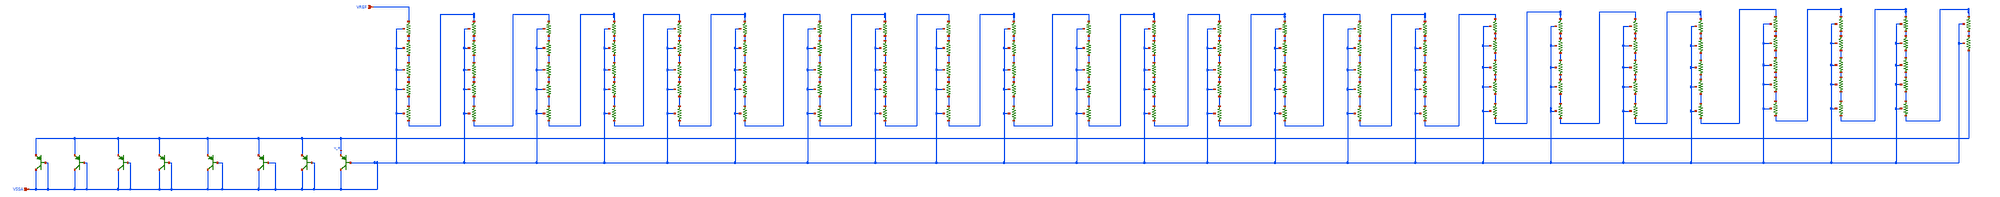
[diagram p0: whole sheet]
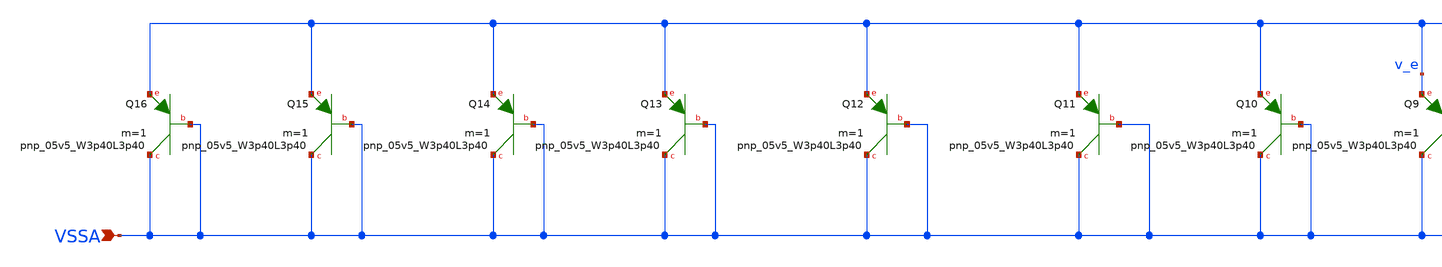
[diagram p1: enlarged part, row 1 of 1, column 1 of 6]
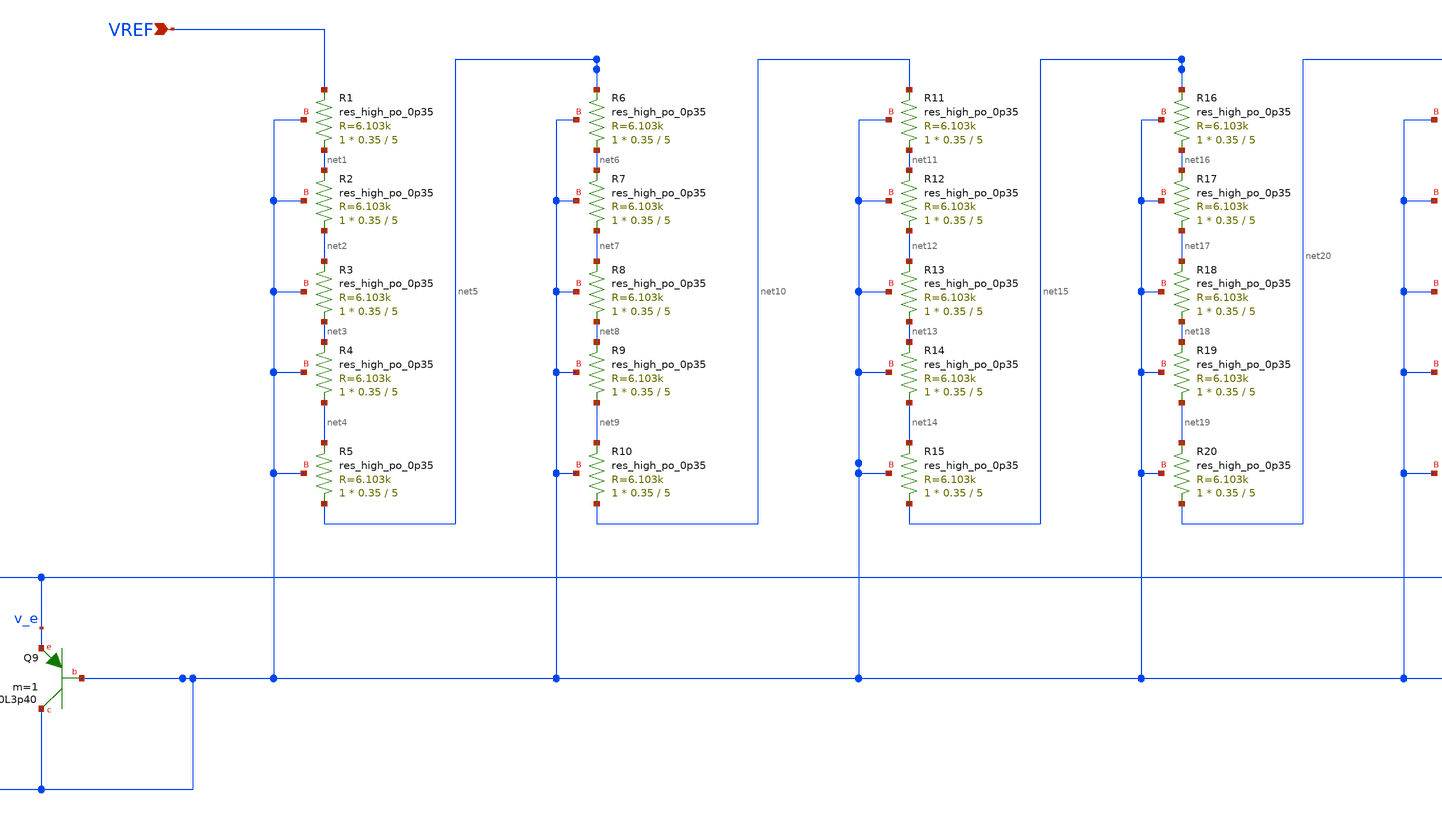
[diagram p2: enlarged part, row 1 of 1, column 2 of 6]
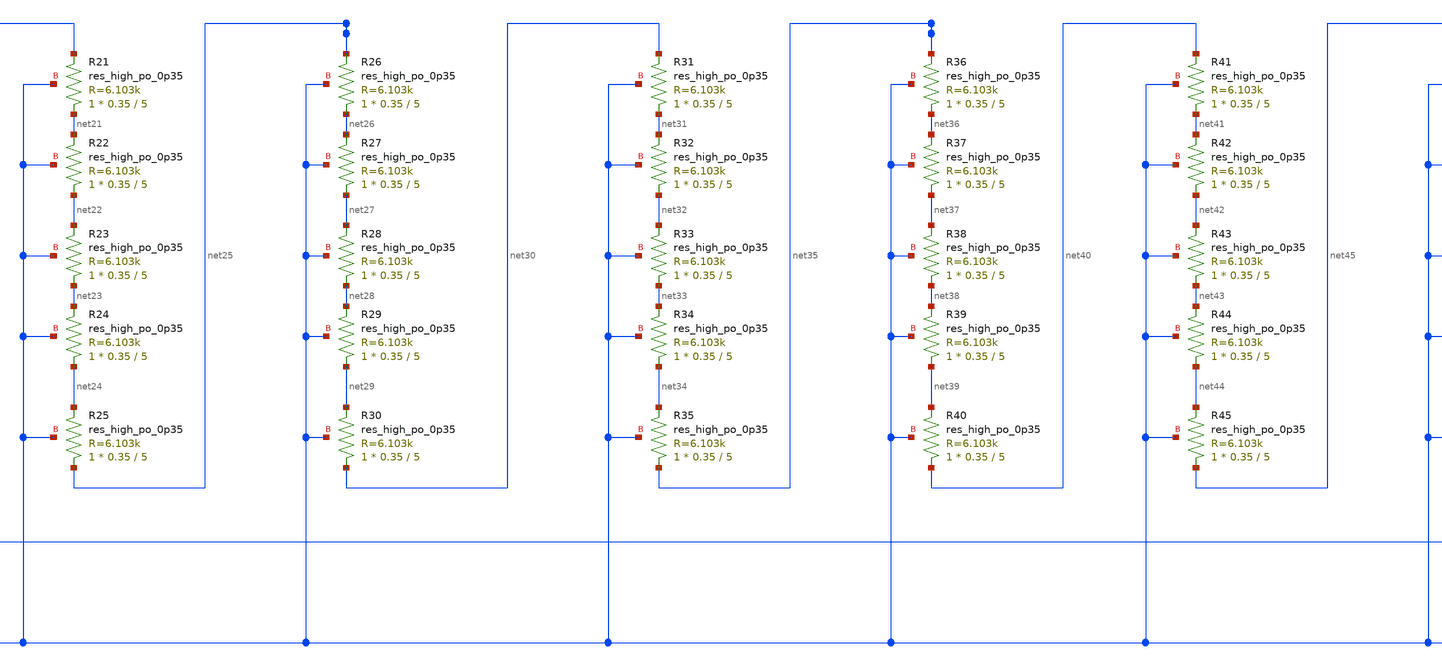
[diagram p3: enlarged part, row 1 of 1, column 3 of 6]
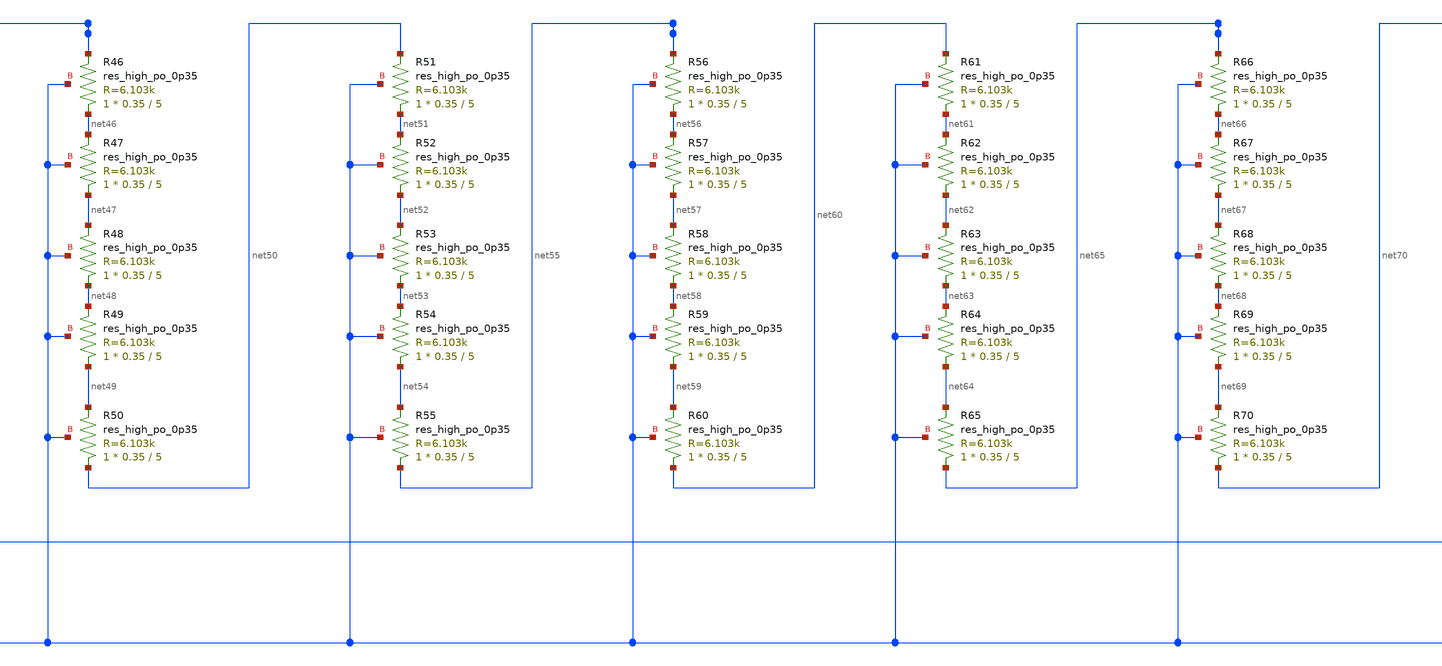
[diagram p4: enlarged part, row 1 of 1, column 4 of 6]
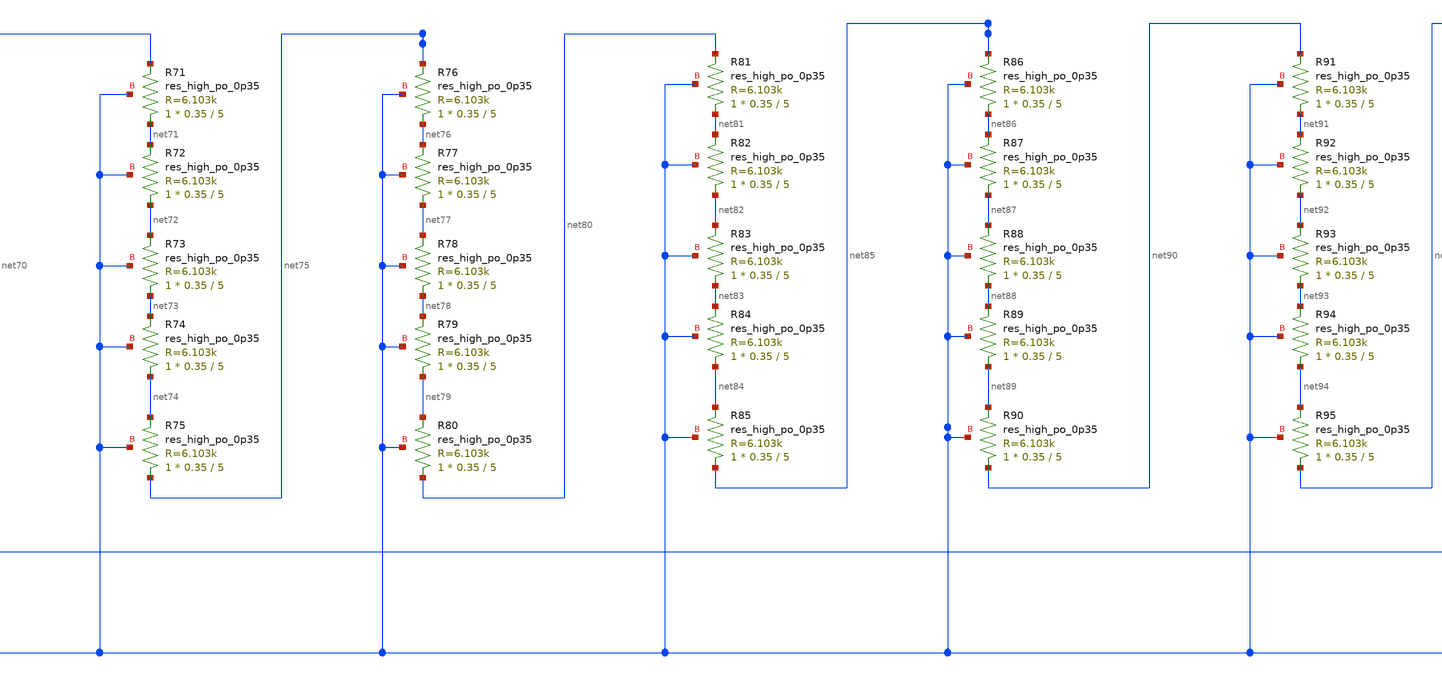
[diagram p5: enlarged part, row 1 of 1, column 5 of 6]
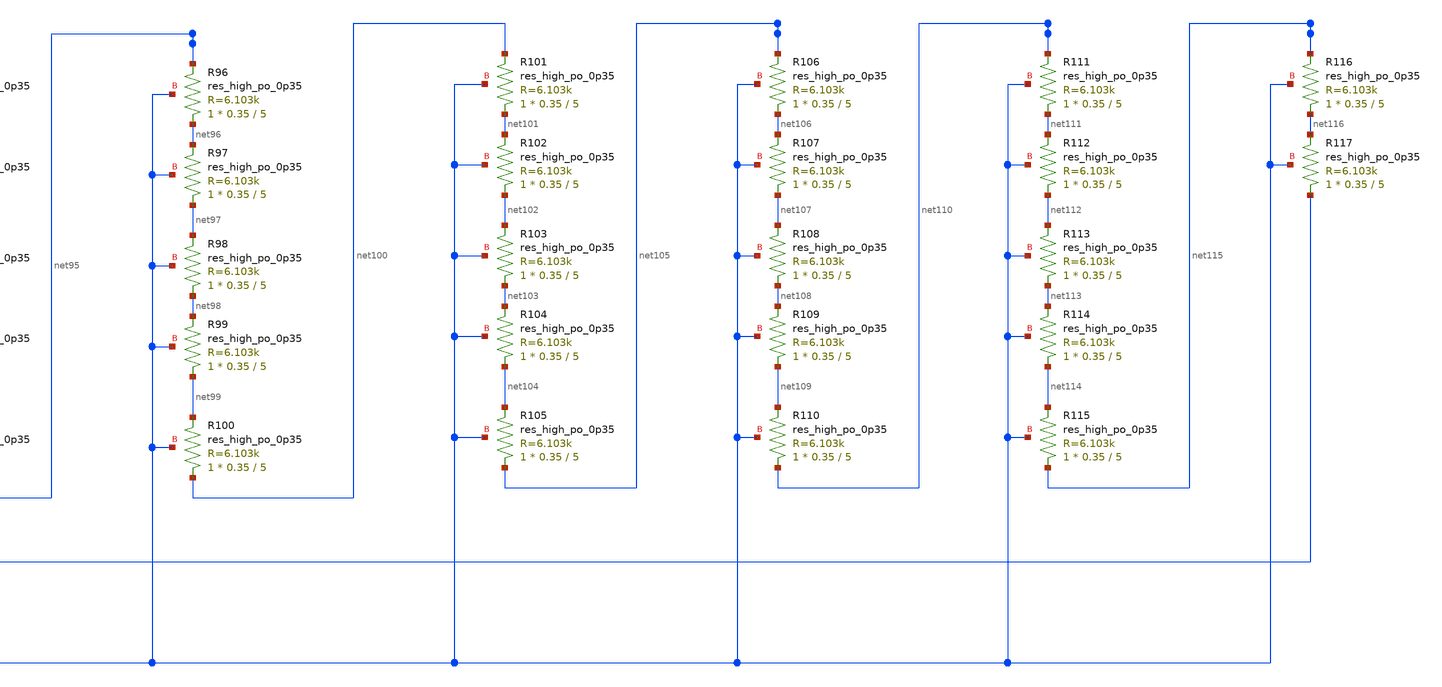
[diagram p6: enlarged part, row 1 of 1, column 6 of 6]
** sch_path: gds/bg2_right_branch_lvs.sch
**.subckt bg2_right_branch_lvs VSSA VREF
*.ipin VSSA
*.ipin VREF
XQ9 VSSA VSSA v_e sky130_fd_pr__pnp_05v5_W3p40L3p40 m=1
XQ10 VSSA VSSA v_e sky130_fd_pr__pnp_05v5_W3p40L3p40 m=1
XQ11 VSSA VSSA v_e sky130_fd_pr__pnp_05v5_W3p40L3p40 m=1
XQ12 VSSA VSSA v_e sky130_fd_pr__pnp_05v5_W3p40L3p40 m=1
XQ13 VSSA VSSA v_e sky130_fd_pr__pnp_05v5_W3p40L3p40 m=1
XQ14 VSSA VSSA v_e sky130_fd_pr__pnp_05v5_W3p40L3p40 m=1
XQ15 VSSA VSSA v_e sky130_fd_pr__pnp_05v5_W3p40L3p40 m=1
XQ16 VSSA VSSA v_e sky130_fd_pr__pnp_05v5_W3p40L3p40 m=1
XR1 net1 VREF VSSA sky130_fd_pr__res_high_po_0p35 L=5 mult=1 m=1
XR2 net2 net1 VSSA sky130_fd_pr__res_high_po_0p35 L=5 mult=1 m=1
XR3 net3 net2 VSSA sky130_fd_pr__res_high_po_0p35 L=5 mult=1 m=1
XR4 net4 net3 VSSA sky130_fd_pr__res_high_po_0p35 L=5 mult=1 m=1
XR5 net5 net4 VSSA sky130_fd_pr__res_high_po_0p35 L=5 mult=1 m=1
XR6 net6 net5 VSSA sky130_fd_pr__res_high_po_0p35 L=5 mult=1 m=1
XR7 net7 net6 VSSA sky130_fd_pr__res_high_po_0p35 L=5 mult=1 m=1
XR8 net8 net7 VSSA sky130_fd_pr__res_high_po_0p35 L=5 mult=1 m=1
XR9 net9 net8 VSSA sky130_fd_pr__res_high_po_0p35 L=5 mult=1 m=1
XR10 net10 net9 VSSA sky130_fd_pr__res_high_po_0p35 L=5 mult=1 m=1
XR11 net11 net10 VSSA sky130_fd_pr__res_high_po_0p35 L=5 mult=1 m=1
XR12 net12 net11 VSSA sky130_fd_pr__res_high_po_0p35 L=5 mult=1 m=1
XR13 net13 net12 VSSA sky130_fd_pr__res_high_po_0p35 L=5 mult=1 m=1
XR14 net14 net13 VSSA sky130_fd_pr__res_high_po_0p35 L=5 mult=1 m=1
XR15 net15 net14 VSSA sky130_fd_pr__res_high_po_0p35 L=5 mult=1 m=1
XR16 net16 net15 VSSA sky130_fd_pr__res_high_po_0p35 L=5 mult=1 m=1
XR17 net17 net16 VSSA sky130_fd_pr__res_high_po_0p35 L=5 mult=1 m=1
XR18 net18 net17 VSSA sky130_fd_pr__res_high_po_0p35 L=5 mult=1 m=1
XR19 net19 net18 VSSA sky130_fd_pr__res_high_po_0p35 L=5 mult=1 m=1
XR20 net20 net19 VSSA sky130_fd_pr__res_high_po_0p35 L=5 mult=1 m=1
XR21 net21 net20 VSSA sky130_fd_pr__res_high_po_0p35 L=5 mult=1 m=1
XR22 net22 net21 VSSA sky130_fd_pr__res_high_po_0p35 L=5 mult=1 m=1
XR23 net23 net22 VSSA sky130_fd_pr__res_high_po_0p35 L=5 mult=1 m=1
XR24 net24 net23 VSSA sky130_fd_pr__res_high_po_0p35 L=5 mult=1 m=1
XR25 net25 net24 VSSA sky130_fd_pr__res_high_po_0p35 L=5 mult=1 m=1
XR26 net26 net25 VSSA sky130_fd_pr__res_high_po_0p35 L=5 mult=1 m=1
XR27 net27 net26 VSSA sky130_fd_pr__res_high_po_0p35 L=5 mult=1 m=1
XR28 net28 net27 VSSA sky130_fd_pr__res_high_po_0p35 L=5 mult=1 m=1
XR29 net29 net28 VSSA sky130_fd_pr__res_high_po_0p35 L=5 mult=1 m=1
XR30 net30 net29 VSSA sky130_fd_pr__res_high_po_0p35 L=5 mult=1 m=1
XR31 net31 net30 VSSA sky130_fd_pr__res_high_po_0p35 L=5 mult=1 m=1
XR32 net32 net31 VSSA sky130_fd_pr__res_high_po_0p35 L=5 mult=1 m=1
XR33 net33 net32 VSSA sky130_fd_pr__res_high_po_0p35 L=5 mult=1 m=1
XR34 net34 net33 VSSA sky130_fd_pr__res_high_po_0p35 L=5 mult=1 m=1
XR35 net35 net34 VSSA sky130_fd_pr__res_high_po_0p35 L=5 mult=1 m=1
XR36 net36 net35 VSSA sky130_fd_pr__res_high_po_0p35 L=5 mult=1 m=1
XR37 net37 net36 VSSA sky130_fd_pr__res_high_po_0p35 L=5 mult=1 m=1
XR38 net38 net37 VSSA sky130_fd_pr__res_high_po_0p35 L=5 mult=1 m=1
XR39 net39 net38 VSSA sky130_fd_pr__res_high_po_0p35 L=5 mult=1 m=1
XR40 net40 net39 VSSA sky130_fd_pr__res_high_po_0p35 L=5 mult=1 m=1
XR41 net41 net40 VSSA sky130_fd_pr__res_high_po_0p35 L=5 mult=1 m=1
XR42 net42 net41 VSSA sky130_fd_pr__res_high_po_0p35 L=5 mult=1 m=1
XR43 net43 net42 VSSA sky130_fd_pr__res_high_po_0p35 L=5 mult=1 m=1
XR44 net44 net43 VSSA sky130_fd_pr__res_high_po_0p35 L=5 mult=1 m=1
XR45 net45 net44 VSSA sky130_fd_pr__res_high_po_0p35 L=5 mult=1 m=1
XR46 net46 net45 VSSA sky130_fd_pr__res_high_po_0p35 L=5 mult=1 m=1
XR47 net47 net46 VSSA sky130_fd_pr__res_high_po_0p35 L=5 mult=1 m=1
XR48 net48 net47 VSSA sky130_fd_pr__res_high_po_0p35 L=5 mult=1 m=1
XR49 net49 net48 VSSA sky130_fd_pr__res_high_po_0p35 L=5 mult=1 m=1
XR50 net50 net49 VSSA sky130_fd_pr__res_high_po_0p35 L=5 mult=1 m=1
XR51 net51 net50 VSSA sky130_fd_pr__res_high_po_0p35 L=5 mult=1 m=1
XR52 net52 net51 VSSA sky130_fd_pr__res_high_po_0p35 L=5 mult=1 m=1
XR53 net53 net52 VSSA sky130_fd_pr__res_high_po_0p35 L=5 mult=1 m=1
XR54 net54 net53 VSSA sky130_fd_pr__res_high_po_0p35 L=5 mult=1 m=1
XR55 net55 net54 VSSA sky130_fd_pr__res_high_po_0p35 L=5 mult=1 m=1
XR56 net56 net55 VSSA sky130_fd_pr__res_high_po_0p35 L=5 mult=1 m=1
XR57 net57 net56 VSSA sky130_fd_pr__res_high_po_0p35 L=5 mult=1 m=1
XR58 net58 net57 VSSA sky130_fd_pr__res_high_po_0p35 L=5 mult=1 m=1
XR59 net59 net58 VSSA sky130_fd_pr__res_high_po_0p35 L=5 mult=1 m=1
XR60 net60 net59 VSSA sky130_fd_pr__res_high_po_0p35 L=5 mult=1 m=1
XR61 net61 net60 VSSA sky130_fd_pr__res_high_po_0p35 L=5 mult=1 m=1
XR62 net62 net61 VSSA sky130_fd_pr__res_high_po_0p35 L=5 mult=1 m=1
XR63 net63 net62 VSSA sky130_fd_pr__res_high_po_0p35 L=5 mult=1 m=1
XR64 net64 net63 VSSA sky130_fd_pr__res_high_po_0p35 L=5 mult=1 m=1
XR65 net65 net64 VSSA sky130_fd_pr__res_high_po_0p35 L=5 mult=1 m=1
XR66 net66 net65 VSSA sky130_fd_pr__res_high_po_0p35 L=5 mult=1 m=1
XR67 net67 net66 VSSA sky130_fd_pr__res_high_po_0p35 L=5 mult=1 m=1
XR68 net68 net67 VSSA sky130_fd_pr__res_high_po_0p35 L=5 mult=1 m=1
XR69 net69 net68 VSSA sky130_fd_pr__res_high_po_0p35 L=5 mult=1 m=1
XR70 net70 net69 VSSA sky130_fd_pr__res_high_po_0p35 L=5 mult=1 m=1
XR71 net71 net70 VSSA sky130_fd_pr__res_high_po_0p35 L=5 mult=1 m=1
XR72 net72 net71 VSSA sky130_fd_pr__res_high_po_0p35 L=5 mult=1 m=1
XR73 net73 net72 VSSA sky130_fd_pr__res_high_po_0p35 L=5 mult=1 m=1
XR74 net74 net73 VSSA sky130_fd_pr__res_high_po_0p35 L=5 mult=1 m=1
XR75 net75 net74 VSSA sky130_fd_pr__res_high_po_0p35 L=5 mult=1 m=1
XR76 net76 net75 VSSA sky130_fd_pr__res_high_po_0p35 L=5 mult=1 m=1
XR77 net77 net76 VSSA sky130_fd_pr__res_high_po_0p35 L=5 mult=1 m=1
XR78 net78 net77 VSSA sky130_fd_pr__res_high_po_0p35 L=5 mult=1 m=1
XR79 net79 net78 VSSA sky130_fd_pr__res_high_po_0p35 L=5 mult=1 m=1
XR80 net80 net79 VSSA sky130_fd_pr__res_high_po_0p35 L=5 mult=1 m=1
XR81 net81 net80 VSSA sky130_fd_pr__res_high_po_0p35 L=5 mult=1 m=1
XR82 net82 net81 VSSA sky130_fd_pr__res_high_po_0p35 L=5 mult=1 m=1
XR83 net83 net82 VSSA sky130_fd_pr__res_high_po_0p35 L=5 mult=1 m=1
XR84 net84 net83 VSSA sky130_fd_pr__res_high_po_0p35 L=5 mult=1 m=1
XR85 net85 net84 VSSA sky130_fd_pr__res_high_po_0p35 L=5 mult=1 m=1
XR86 net86 net85 VSSA sky130_fd_pr__res_high_po_0p35 L=5 mult=1 m=1
XR87 net87 net86 VSSA sky130_fd_pr__res_high_po_0p35 L=5 mult=1 m=1
XR88 net88 net87 VSSA sky130_fd_pr__res_high_po_0p35 L=5 mult=1 m=1
XR89 net89 net88 VSSA sky130_fd_pr__res_high_po_0p35 L=5 mult=1 m=1
XR90 net90 net89 VSSA sky130_fd_pr__res_high_po_0p35 L=5 mult=1 m=1
XR91 net91 net90 VSSA sky130_fd_pr__res_high_po_0p35 L=5 mult=1 m=1
XR92 net92 net91 VSSA sky130_fd_pr__res_high_po_0p35 L=5 mult=1 m=1
XR93 net93 net92 VSSA sky130_fd_pr__res_high_po_0p35 L=5 mult=1 m=1
XR94 net94 net93 VSSA sky130_fd_pr__res_high_po_0p35 L=5 mult=1 m=1
XR95 net95 net94 VSSA sky130_fd_pr__res_high_po_0p35 L=5 mult=1 m=1
XR96 net96 net95 VSSA sky130_fd_pr__res_high_po_0p35 L=5 mult=1 m=1
XR97 net97 net96 VSSA sky130_fd_pr__res_high_po_0p35 L=5 mult=1 m=1
XR98 net98 net97 VSSA sky130_fd_pr__res_high_po_0p35 L=5 mult=1 m=1
XR99 net99 net98 VSSA sky130_fd_pr__res_high_po_0p35 L=5 mult=1 m=1
XR100 net100 net99 VSSA sky130_fd_pr__res_high_po_0p35 L=5 mult=1 m=1
XR101 net101 net100 VSSA sky130_fd_pr__res_high_po_0p35 L=5 mult=1 m=1
XR102 net102 net101 VSSA sky130_fd_pr__res_high_po_0p35 L=5 mult=1 m=1
XR103 net103 net102 VSSA sky130_fd_pr__res_high_po_0p35 L=5 mult=1 m=1
XR104 net104 net103 VSSA sky130_fd_pr__res_high_po_0p35 L=5 mult=1 m=1
XR105 net105 net104 VSSA sky130_fd_pr__res_high_po_0p35 L=5 mult=1 m=1
XR106 net106 net105 VSSA sky130_fd_pr__res_high_po_0p35 L=5 mult=1 m=1
XR107 net107 net106 VSSA sky130_fd_pr__res_high_po_0p35 L=5 mult=1 m=1
XR108 net108 net107 VSSA sky130_fd_pr__res_high_po_0p35 L=5 mult=1 m=1
XR109 net109 net108 VSSA sky130_fd_pr__res_high_po_0p35 L=5 mult=1 m=1
XR110 net110 net109 VSSA sky130_fd_pr__res_high_po_0p35 L=5 mult=1 m=1
XR111 net111 net110 VSSA sky130_fd_pr__res_high_po_0p35 L=5 mult=1 m=1
XR112 net112 net111 VSSA sky130_fd_pr__res_high_po_0p35 L=5 mult=1 m=1
XR113 net113 net112 VSSA sky130_fd_pr__res_high_po_0p35 L=5 mult=1 m=1
XR114 net114 net113 VSSA sky130_fd_pr__res_high_po_0p35 L=5 mult=1 m=1
XR115 net115 net114 VSSA sky130_fd_pr__res_high_po_0p35 L=5 mult=1 m=1
XR116 net116 net115 VSSA sky130_fd_pr__res_high_po_0p35 L=5 mult=1 m=1
XR117 v_e net116 VSSA sky130_fd_pr__res_high_po_0p35 L=5 mult=1 m=1
**.ends
.end
